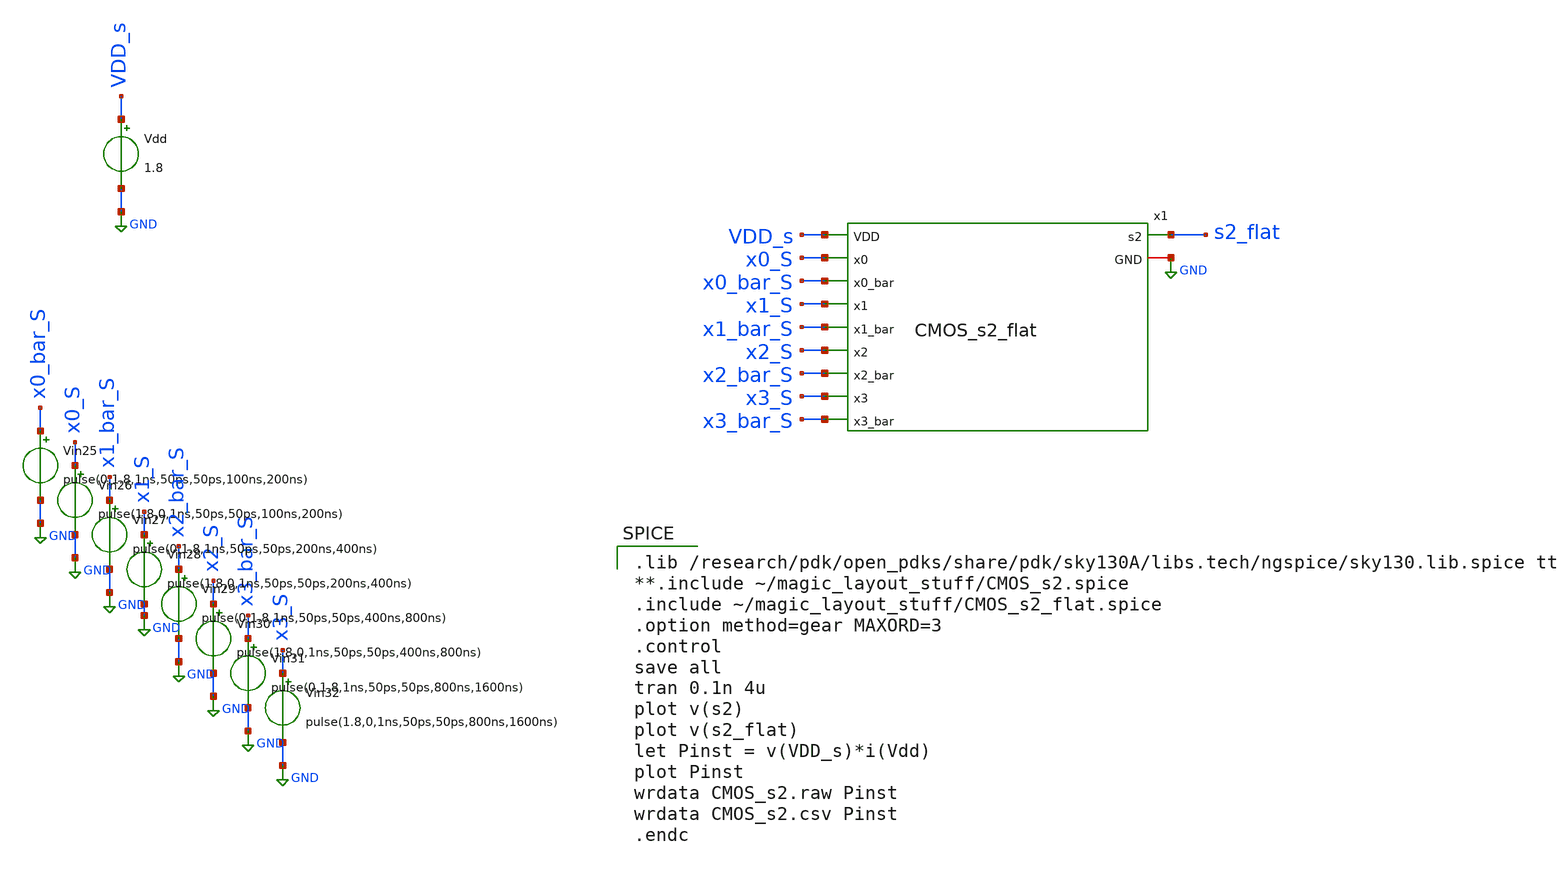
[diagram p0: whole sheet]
** sch_path: skywater_stuff/CMOS_s2_sim.sch
**.subckt CMOS_s2_sim
Vdd VDD_s GND 1.8
Vin25 x0_bar_S GND pulse(0,1.8,1ns,50ps,50ps,100ns,200ns)
Vin26 x0_S GND pulse(1.8,0,1ns,50ps,50ps,100ns,200ns)
Vin27 x1_bar_S GND pulse(0,1.8,1ns,50ps,50ps,200ns,400ns)
Vin28 x1_S GND pulse(1.8,0,1ns,50ps,50ps,200ns,400ns)
Vin29 x2_bar_S GND pulse(0,1.8,1ns,50ps,50ps,400ns,800ns)
Vin30 x2_S GND pulse(1.8,0,1ns,50ps,50ps,400ns,800ns)
Vin31 x3_bar_S GND pulse(0,1.8,1ns,50ps,50ps,800ns,1600ns)
Vin32 x3_S GND pulse(1.8,0,1ns,50ps,50ps,800ns,1600ns)
x1 GND x0_S x0_bar_S x1_S x1_bar_S x2_S x2_bar_S x3_S x3_bar_S s2_flat VDD_s CMOS_s2_flat
**** begin user architecture code

.lib /research/pdk/open_pdks/share/pdk/sky130A/libs.tech/ngspice/sky130.lib.spice tt
**.include ~/magic_layout_stuff/CMOS_s2.spice
.include ~/magic_layout_stuff/CMOS_s2_flat.spice
.option method=gear MAXORD=3
.control
save all
tran 0.1n 4u
plot v(s2)
plot v(s2_flat)
let Pinst = v(VDD_s)*i(Vdd)
plot Pinst
wrdata CMOS_s2.raw Pinst
wrdata CMOS_s2.csv Pinst
.endc


**** end user architecture code
**.ends
.GLOBAL GND
.end
